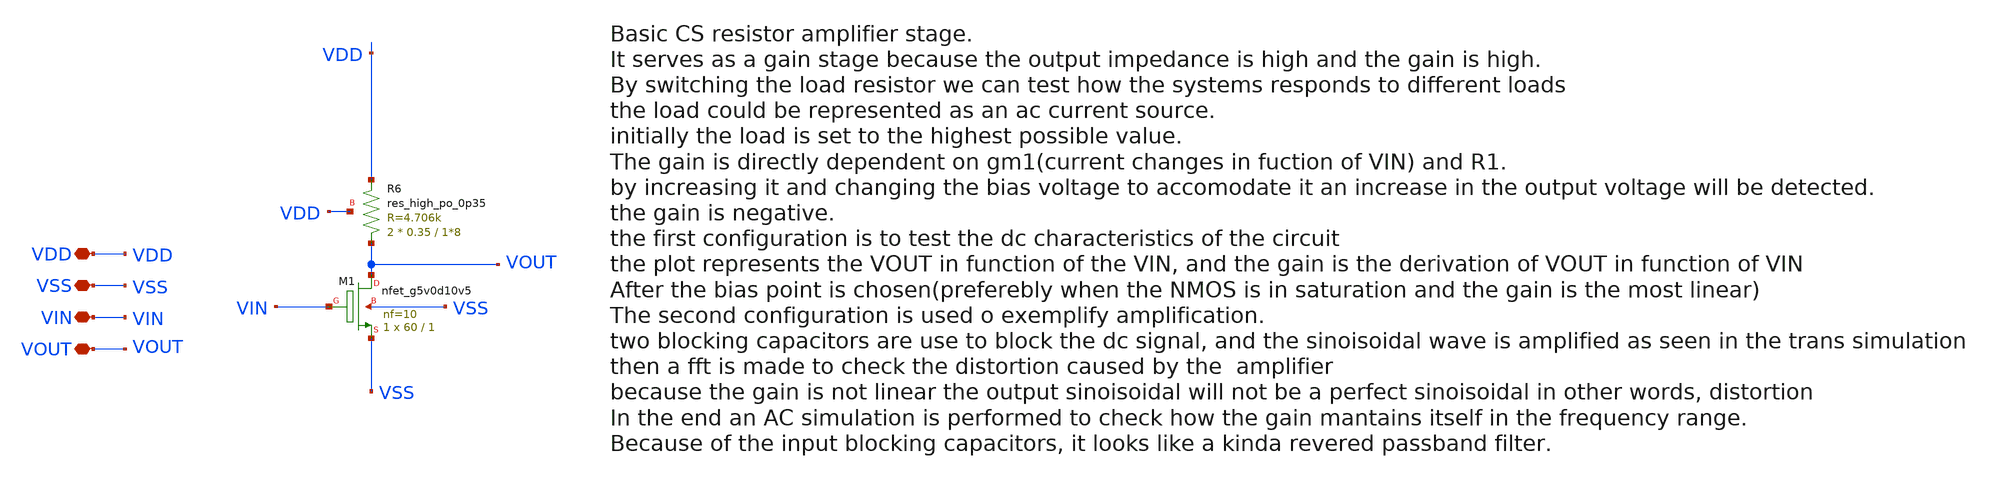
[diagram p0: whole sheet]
** sch_path: old stuff/amplifiers/single_stage_amps/basic_stages/cs_resistor_stage/cs_resistor_stage.sch
**.subckt cs_resistor_stage VDD VSS VIN VOUT
*.iopin VDD
*.iopin VSS
*.iopin VIN
*.iopin VOUT
XM1 VOUT VIN VSS VSS sky130_fd_pr__nfet_g5v0d10v5 L=1 W=60 nf=10 ad='int((nf+1)/2) * W/nf * 0.29' as='int((nf+2)/2) * W/nf * 0.29'
+ pd='2*int((nf+1)/2) * (W/nf + 0.29)' ps='2*int((nf+2)/2) * (W/nf + 0.29)' nrd='0.29 / W' nrs='0.29 / W'
+ sa=0 sb=0 sd=0 mult=1 m=1
XR6 VOUT VDD VDD sky130_fd_pr__res_high_po_0p35 L=1*8 mult=2 m=2
**.ends
.end
